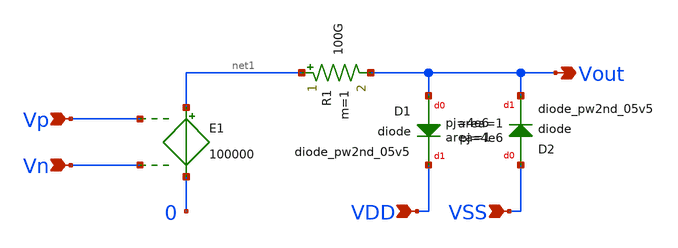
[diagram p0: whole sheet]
** sch_path: testing/Ideal_Opamp.sch
**.subckt Ideal_Opamp Vp Vn Vout VDD VSS
*.ipin Vp
*.ipin Vn
*.opin Vout
*.ipin VDD
*.ipin VSS
E1 net1 0 Vp Vn 100000
R1 net1 Vout 100G m=1
XD1 Vout VDD sky130_fd_pr__diode_pw2nd_05v5 area=1 pj=4e6
XD2 VSS Vout sky130_fd_pr__diode_pw2nd_05v5 area=1 pj=4e6
**.ends
.end
